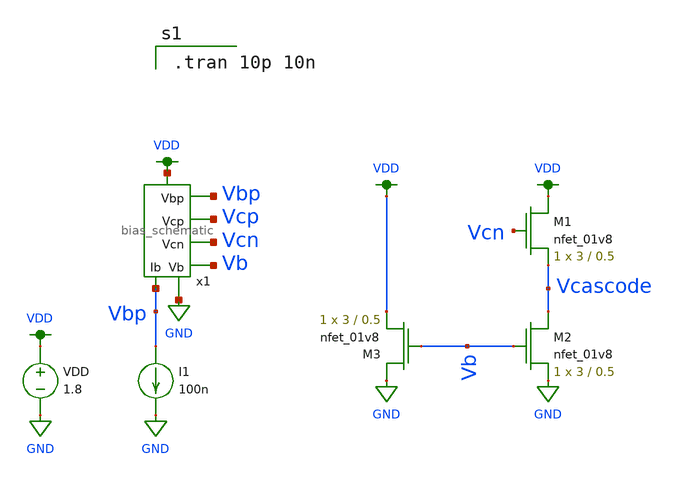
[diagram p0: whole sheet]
** sch_path: mp3/xschem/test_bias.sch
**.subckt test_bias
x1 VDD Vbp Vbp Vcp Vcn GND Vb bias_schematic
I1 Vbp GND 100n
VDD VDD GND 1.8
XM1 VDD Vcn Vcascode GND sky130_fd_pr__nfet_01v8 L=0.5 W=3 nf=1 ad='int((nf+1)/2) * W/nf * 0.29' as='int((nf+2)/2) * W/nf * 0.29'
+ pd='2*int((nf+1)/2) * (W/nf + 0.29)' ps='2*int((nf+2)/2) * (W/nf + 0.29)' nrd='0.29 / W' nrs='0.29 / W'
+ sa=0 sb=0 sd=0 mult=1 m=1
XM2 Vcascode Vb GND GND sky130_fd_pr__nfet_01v8 L=0.5 W=3 nf=1 ad='int((nf+1)/2) * W/nf * 0.29' as='int((nf+2)/2) * W/nf * 0.29'
+ pd='2*int((nf+1)/2) * (W/nf + 0.29)' ps='2*int((nf+2)/2) * (W/nf + 0.29)' nrd='0.29 / W' nrs='0.29 / W'
+ sa=0 sb=0 sd=0 mult=1 m=1
XM3 GND Vb VDD GND sky130_fd_pr__nfet_01v8 L=0.5 W=3 nf=1 ad='int((nf+1)/2) * W/nf * 0.29' as='int((nf+2)/2) * W/nf * 0.29'
+ pd='2*int((nf+1)/2) * (W/nf + 0.29)' ps='2*int((nf+2)/2) * (W/nf + 0.29)' nrd='0.29 / W' nrs='0.29 / W'
+ sa=0 sb=0 sd=0 mult=1 m=1
**** begin user architecture code

.option wnflag=1
.lib ~/skywater/skywater-pdk/libraries/sky130_fd_pr_ngspice/latest/models/sky130.lib.spice tt


.tran 10p 10n

**** end user architecture code
**.ends

* expanding   symbol:  /home/madvlsi/dev/git/vlsi/mp3/xschem/bias_schematic.sym # of pins=7
** sym_path: mp3/debug_files/bias_schematic.sym
** sch_path: mp3/debug_files/bias_schematic.sch
.subckt bias_schematic VP Vbp Ib Vcp Vcn VN Vb
*.iopin VP
*.iopin VN
*.iopin Ib
*.opin Vcp
*.opin Vbp
*.opin Vcn
*.opin Vb
XM1a net2 net2 net1 GND sky130_fd_pr__nfet_01v8 L=0.5 W=30 nf=1 ad='int((nf+1)/2) * W/nf * 0.29' as='int((nf+2)/2) * W/nf * 0.29'
+ pd='2*int((nf+1)/2) * (W/nf + 0.29)' ps='2*int((nf+2)/2) * (W/nf + 0.29)' nrd='0.29 / W' nrs='0.29 / W'
+ sa=0 sb=0 sd=0 mult=1 m=1
XM1b net2 net2 net1 GND sky130_fd_pr__nfet_01v8 L=0.5 W=30 nf=1 ad='int((nf+1)/2) * W/nf * 0.29' as='int((nf+2)/2) * W/nf * 0.29'
+ pd='2*int((nf+1)/2) * (W/nf + 0.29)' ps='2*int((nf+2)/2) * (W/nf + 0.29)' nrd='0.29 / W' nrs='0.29 / W'
+ sa=0 sb=0 sd=0 mult=1 m=1
XM1c net2 net2 net1 GND sky130_fd_pr__nfet_01v8 L=0.5 W=30 nf=1 ad='int((nf+1)/2) * W/nf * 0.29' as='int((nf+2)/2) * W/nf * 0.29'
+ pd='2*int((nf+1)/2) * (W/nf + 0.29)' ps='2*int((nf+2)/2) * (W/nf + 0.29)' nrd='0.29 / W' nrs='0.29 / W'
+ sa=0 sb=0 sd=0 mult=1 m=1
XM1d net2 net2 net1 GND sky130_fd_pr__nfet_01v8 L=0.5 W=30 nf=1 ad='int((nf+1)/2) * W/nf * 0.29' as='int((nf+2)/2) * W/nf * 0.29'
+ pd='2*int((nf+1)/2) * (W/nf + 0.29)' ps='2*int((nf+2)/2) * (W/nf + 0.29)' nrd='0.29 / W' nrs='0.29 / W'
+ sa=0 sb=0 sd=0 mult=1 m=1
XM2a VN net2 net1 GND sky130_fd_pr__nfet_01v8 L=0.5 W=3 nf=1 ad='int((nf+1)/2) * W/nf * 0.29' as='int((nf+2)/2) * W/nf * 0.29'
+ pd='2*int((nf+1)/2) * (W/nf + 0.29)' ps='2*int((nf+2)/2) * (W/nf + 0.29)' nrd='0.29 / W' nrs='0.29 / W'
+ sa=0 sb=0 sd=0 mult=1 m=1
XM2b VN net2 net1 GND sky130_fd_pr__nfet_01v8 L=0.5 W=3 nf=1 ad='int((nf+1)/2) * W/nf * 0.29' as='int((nf+2)/2) * W/nf * 0.29'
+ pd='2*int((nf+1)/2) * (W/nf + 0.29)' ps='2*int((nf+2)/2) * (W/nf + 0.29)' nrd='0.29 / W' nrs='0.29 / W'
+ sa=0 sb=0 sd=0 mult=1 m=1
XM2c VN net2 net1 GND sky130_fd_pr__nfet_01v8 L=0.5 W=3 nf=1 ad='int((nf+1)/2) * W/nf * 0.29' as='int((nf+2)/2) * W/nf * 0.29'
+ pd='2*int((nf+1)/2) * (W/nf + 0.29)' ps='2*int((nf+2)/2) * (W/nf + 0.29)' nrd='0.29 / W' nrs='0.29 / W'
+ sa=0 sb=0 sd=0 mult=1 m=1
XM2d VN net2 net1 GND sky130_fd_pr__nfet_01v8 L=0.5 W=3 nf=1 ad='int((nf+1)/2) * W/nf * 0.29' as='int((nf+2)/2) * W/nf * 0.29'
+ pd='2*int((nf+1)/2) * (W/nf + 0.29)' ps='2*int((nf+2)/2) * (W/nf + 0.29)' nrd='0.29 / W' nrs='0.29 / W'
+ sa=0 sb=0 sd=0 mult=1 m=1
XM3a net2 Ib VP VDD sky130_fd_pr__pfet_01v8 L=0.5 W=3 nf=1 ad='int((nf+1)/2) * W/nf * 0.29' as='int((nf+2)/2) * W/nf * 0.29'
+ pd='2*int((nf+1)/2) * (W/nf + 0.29)' ps='2*int((nf+2)/2) * (W/nf + 0.29)' nrd='0.29 / W' nrs='0.29 / W'
+ sa=0 sb=0 sd=0 mult=1 m=1
XM3b net2 Ib VP VDD sky130_fd_pr__pfet_01v8 L=0.5 W=3 nf=1 ad='int((nf+1)/2) * W/nf * 0.29' as='int((nf+2)/2) * W/nf * 0.29'
+ pd='2*int((nf+1)/2) * (W/nf + 0.29)' ps='2*int((nf+2)/2) * (W/nf + 0.29)' nrd='0.29 / W' nrs='0.29 / W'
+ sa=0 sb=0 sd=0 mult=1 m=1
XM3c net2 Ib VP VDD sky130_fd_pr__pfet_01v8 L=0.5 W=3 nf=1 ad='int((nf+1)/2) * W/nf * 0.29' as='int((nf+2)/2) * W/nf * 0.29'
+ pd='2*int((nf+1)/2) * (W/nf + 0.29)' ps='2*int((nf+2)/2) * (W/nf + 0.29)' nrd='0.29 / W' nrs='0.29 / W'
+ sa=0 sb=0 sd=0 mult=1 m=1
XM3d net2 Ib VP VDD sky130_fd_pr__pfet_01v8 L=0.5 W=3 nf=1 ad='int((nf+1)/2) * W/nf * 0.29' as='int((nf+2)/2) * W/nf * 0.29'
+ pd='2*int((nf+1)/2) * (W/nf + 0.29)' ps='2*int((nf+2)/2) * (W/nf + 0.29)' nrd='0.29 / W' nrs='0.29 / W'
+ sa=0 sb=0 sd=0 mult=1 m=1
XM4a Vcn Ib VP VDD sky130_fd_pr__pfet_01v8 L=0.5 W=30 nf=1 ad='int((nf+1)/2) * W/nf * 0.29' as='int((nf+2)/2) * W/nf * 0.29'
+ pd='2*int((nf+1)/2) * (W/nf + 0.29)' ps='2*int((nf+2)/2) * (W/nf + 0.29)' nrd='0.29 / W' nrs='0.29 / W'
+ sa=0 sb=0 sd=0 mult=1 m=1
XM4b Vcn Ib VP VDD sky130_fd_pr__pfet_01v8 L=0.5 W=30 nf=1 ad='int((nf+1)/2) * W/nf * 0.29' as='int((nf+2)/2) * W/nf * 0.29'
+ pd='2*int((nf+1)/2) * (W/nf + 0.29)' ps='2*int((nf+2)/2) * (W/nf + 0.29)' nrd='0.29 / W' nrs='0.29 / W'
+ sa=0 sb=0 sd=0 mult=1 m=1
XM4c Vcn Ib VP VDD sky130_fd_pr__pfet_01v8 L=0.5 W=30 nf=1 ad='int((nf+1)/2) * W/nf * 0.29' as='int((nf+2)/2) * W/nf * 0.29'
+ pd='2*int((nf+1)/2) * (W/nf + 0.29)' ps='2*int((nf+2)/2) * (W/nf + 0.29)' nrd='0.29 / W' nrs='0.29 / W'
+ sa=0 sb=0 sd=0 mult=1 m=1
XM4d Vcn Ib VP VDD sky130_fd_pr__pfet_01v8 L=0.5 W=30 nf=1 ad='int((nf+1)/2) * W/nf * 0.29' as='int((nf+2)/2) * W/nf * 0.29'
+ pd='2*int((nf+1)/2) * (W/nf + 0.29)' ps='2*int((nf+2)/2) * (W/nf + 0.29)' nrd='0.29 / W' nrs='0.29 / W'
+ sa=0 sb=0 sd=0 mult=1 m=1
XM11a Ib Ib VP VDD sky130_fd_pr__pfet_01v8 L=0.5 W=3 nf=1 ad='int((nf+1)/2) * W/nf * 0.29' as='int((nf+2)/2) * W/nf * 0.29'
+ pd='2*int((nf+1)/2) * (W/nf + 0.29)' ps='2*int((nf+2)/2) * (W/nf + 0.29)' nrd='0.29 / W' nrs='0.29 / W'
+ sa=0 sb=0 sd=0 mult=1 m=1
XM11b Ib Ib VP VDD sky130_fd_pr__pfet_01v8 L=0.5 W=3 nf=1 ad='int((nf+1)/2) * W/nf * 0.29' as='int((nf+2)/2) * W/nf * 0.29'
+ pd='2*int((nf+1)/2) * (W/nf + 0.29)' ps='2*int((nf+2)/2) * (W/nf + 0.29)' nrd='0.29 / W' nrs='0.29 / W'
+ sa=0 sb=0 sd=0 mult=1 m=1
XM11c Ib Ib VP VDD sky130_fd_pr__pfet_01v8 L=0.5 W=3 nf=1 ad='int((nf+1)/2) * W/nf * 0.29' as='int((nf+2)/2) * W/nf * 0.29'
+ pd='2*int((nf+1)/2) * (W/nf + 0.29)' ps='2*int((nf+2)/2) * (W/nf + 0.29)' nrd='0.29 / W' nrs='0.29 / W'
+ sa=0 sb=0 sd=0 mult=1 m=1
XM11d Ib Ib VP VDD sky130_fd_pr__pfet_01v8 L=0.5 W=3 nf=1 ad='int((nf+1)/2) * W/nf * 0.29' as='int((nf+2)/2) * W/nf * 0.29'
+ pd='2*int((nf+1)/2) * (W/nf + 0.29)' ps='2*int((nf+2)/2) * (W/nf + 0.29)' nrd='0.29 / W' nrs='0.29 / W'
+ sa=0 sb=0 sd=0 mult=1 m=1
XM5a net1 Vcn Vcn GND sky130_fd_pr__nfet_01v8 L=0.5 W=30 nf=1 ad='int((nf+1)/2) * W/nf * 0.29' as='int((nf+2)/2) * W/nf * 0.29'
+ pd='2*int((nf+1)/2) * (W/nf + 0.29)' ps='2*int((nf+2)/2) * (W/nf + 0.29)' nrd='0.29 / W' nrs='0.29 / W'
+ sa=0 sb=0 sd=0 mult=1 m=1
XM5b net1 Vcn Vcn GND sky130_fd_pr__nfet_01v8 L=0.5 W=30 nf=1 ad='int((nf+1)/2) * W/nf * 0.29' as='int((nf+2)/2) * W/nf * 0.29'
+ pd='2*int((nf+1)/2) * (W/nf + 0.29)' ps='2*int((nf+2)/2) * (W/nf + 0.29)' nrd='0.29 / W' nrs='0.29 / W'
+ sa=0 sb=0 sd=0 mult=1 m=1
XM5c net1 Vcn Vcn GND sky130_fd_pr__nfet_01v8 L=0.5 W=30 nf=1 ad='int((nf+1)/2) * W/nf * 0.29' as='int((nf+2)/2) * W/nf * 0.29'
+ pd='2*int((nf+1)/2) * (W/nf + 0.29)' ps='2*int((nf+2)/2) * (W/nf + 0.29)' nrd='0.29 / W' nrs='0.29 / W'
+ sa=0 sb=0 sd=0 mult=1 m=1
XM5d net1 Vcn Vcn GND sky130_fd_pr__nfet_01v8 L=0.5 W=30 nf=1 ad='int((nf+1)/2) * W/nf * 0.29' as='int((nf+2)/2) * W/nf * 0.29'
+ pd='2*int((nf+1)/2) * (W/nf + 0.29)' ps='2*int((nf+2)/2) * (W/nf + 0.29)' nrd='0.29 / W' nrs='0.29 / W'
+ sa=0 sb=0 sd=0 mult=1 m=1
XM8a VN Vb net3 GND sky130_fd_pr__nfet_01v8 L=0.5 W=3 nf=1 ad='int((nf+1)/2) * W/nf * 0.29' as='int((nf+2)/2) * W/nf * 0.29'
+ pd='2*int((nf+1)/2) * (W/nf + 0.29)' ps='2*int((nf+2)/2) * (W/nf + 0.29)' nrd='0.29 / W' nrs='0.29 / W'
+ sa=0 sb=0 sd=0 mult=1 m=1
XM8b VN Vb net3 GND sky130_fd_pr__nfet_01v8 L=0.5 W=3 nf=1 ad='int((nf+1)/2) * W/nf * 0.29' as='int((nf+2)/2) * W/nf * 0.29'
+ pd='2*int((nf+1)/2) * (W/nf + 0.29)' ps='2*int((nf+2)/2) * (W/nf + 0.29)' nrd='0.29 / W' nrs='0.29 / W'
+ sa=0 sb=0 sd=0 mult=1 m=1
XM8c VN Vb net3 GND sky130_fd_pr__nfet_01v8 L=0.5 W=3 nf=1 ad='int((nf+1)/2) * W/nf * 0.29' as='int((nf+2)/2) * W/nf * 0.29'
+ pd='2*int((nf+1)/2) * (W/nf + 0.29)' ps='2*int((nf+2)/2) * (W/nf + 0.29)' nrd='0.29 / W' nrs='0.29 / W'
+ sa=0 sb=0 sd=0 mult=1 m=1
XM8d VN Vb net3 GND sky130_fd_pr__nfet_01v8 L=0.5 W=3 nf=1 ad='int((nf+1)/2) * W/nf * 0.29' as='int((nf+2)/2) * W/nf * 0.29'
+ pd='2*int((nf+1)/2) * (W/nf + 0.29)' ps='2*int((nf+2)/2) * (W/nf + 0.29)' nrd='0.29 / W' nrs='0.29 / W'
+ sa=0 sb=0 sd=0 mult=1 m=1
XM6a net3 net3 net4 VDD sky130_fd_pr__pfet_01v8 L=0.5 W=30 nf=1 ad='int((nf+1)/2) * W/nf * 0.29' as='int((nf+2)/2) * W/nf * 0.29'
+ pd='2*int((nf+1)/2) * (W/nf + 0.29)' ps='2*int((nf+2)/2) * (W/nf + 0.29)' nrd='0.29 / W' nrs='0.29 / W'
+ sa=0 sb=0 sd=0 mult=1 m=1
XM6b net3 net3 net4 VDD sky130_fd_pr__pfet_01v8 L=0.5 W=30 nf=1 ad='int((nf+1)/2) * W/nf * 0.29' as='int((nf+2)/2) * W/nf * 0.29'
+ pd='2*int((nf+1)/2) * (W/nf + 0.29)' ps='2*int((nf+2)/2) * (W/nf + 0.29)' nrd='0.29 / W' nrs='0.29 / W'
+ sa=0 sb=0 sd=0 mult=1 m=1
XM6c net3 net3 net4 VDD sky130_fd_pr__pfet_01v8 L=0.5 W=30 nf=1 ad='int((nf+1)/2) * W/nf * 0.29' as='int((nf+2)/2) * W/nf * 0.29'
+ pd='2*int((nf+1)/2) * (W/nf + 0.29)' ps='2*int((nf+2)/2) * (W/nf + 0.29)' nrd='0.29 / W' nrs='0.29 / W'
+ sa=0 sb=0 sd=0 mult=1 m=1
XM6d net3 net3 net4 VDD sky130_fd_pr__pfet_01v8 L=0.5 W=30 nf=1 ad='int((nf+1)/2) * W/nf * 0.29' as='int((nf+2)/2) * W/nf * 0.29'
+ pd='2*int((nf+1)/2) * (W/nf + 0.29)' ps='2*int((nf+2)/2) * (W/nf + 0.29)' nrd='0.29 / W' nrs='0.29 / W'
+ sa=0 sb=0 sd=0 mult=1 m=1
XM7a net4 net3 VP VDD sky130_fd_pr__pfet_01v8 L=0.5 W=3 nf=1 ad='int((nf+1)/2) * W/nf * 0.29' as='int((nf+2)/2) * W/nf * 0.29'
+ pd='2*int((nf+1)/2) * (W/nf + 0.29)' ps='2*int((nf+2)/2) * (W/nf + 0.29)' nrd='0.29 / W' nrs='0.29 / W'
+ sa=0 sb=0 sd=0 mult=1 m=1
XM7b net4 net3 VP VDD sky130_fd_pr__pfet_01v8 L=0.5 W=3 nf=1 ad='int((nf+1)/2) * W/nf * 0.29' as='int((nf+2)/2) * W/nf * 0.29'
+ pd='2*int((nf+1)/2) * (W/nf + 0.29)' ps='2*int((nf+2)/2) * (W/nf + 0.29)' nrd='0.29 / W' nrs='0.29 / W'
+ sa=0 sb=0 sd=0 mult=1 m=1
XM7c net4 net3 VP VDD sky130_fd_pr__pfet_01v8 L=0.5 W=3 nf=1 ad='int((nf+1)/2) * W/nf * 0.29' as='int((nf+2)/2) * W/nf * 0.29'
+ pd='2*int((nf+1)/2) * (W/nf + 0.29)' ps='2*int((nf+2)/2) * (W/nf + 0.29)' nrd='0.29 / W' nrs='0.29 / W'
+ sa=0 sb=0 sd=0 mult=1 m=1
XM7d net4 net3 VP VDD sky130_fd_pr__pfet_01v8 L=0.5 W=3 nf=1 ad='int((nf+1)/2) * W/nf * 0.29' as='int((nf+2)/2) * W/nf * 0.29'
+ pd='2*int((nf+1)/2) * (W/nf + 0.29)' ps='2*int((nf+2)/2) * (W/nf + 0.29)' nrd='0.29 / W' nrs='0.29 / W'
+ sa=0 sb=0 sd=0 mult=1 m=1
XM10d net4 Vcp Vcp VDD sky130_fd_pr__pfet_01v8 L=0.5 W=30 nf=1 ad='int((nf+1)/2) * W/nf * 0.29' as='int((nf+2)/2) * W/nf * 0.29'
+ pd='2*int((nf+1)/2) * (W/nf + 0.29)' ps='2*int((nf+2)/2) * (W/nf + 0.29)' nrd='0.29 / W' nrs='0.29 / W'
+ sa=0 sb=0 sd=0 mult=1 m=1
XM10c net4 Vcp Vcp VDD sky130_fd_pr__pfet_01v8 L=0.5 W=30 nf=1 ad='int((nf+1)/2) * W/nf * 0.29' as='int((nf+2)/2) * W/nf * 0.29'
+ pd='2*int((nf+1)/2) * (W/nf + 0.29)' ps='2*int((nf+2)/2) * (W/nf + 0.29)' nrd='0.29 / W' nrs='0.29 / W'
+ sa=0 sb=0 sd=0 mult=1 m=1
XM10b net4 Vcp Vcp VDD sky130_fd_pr__pfet_01v8 L=0.5 W=30 nf=1 ad='int((nf+1)/2) * W/nf * 0.29' as='int((nf+2)/2) * W/nf * 0.29'
+ pd='2*int((nf+1)/2) * (W/nf + 0.29)' ps='2*int((nf+2)/2) * (W/nf + 0.29)' nrd='0.29 / W' nrs='0.29 / W'
+ sa=0 sb=0 sd=0 mult=1 m=1
XM10a net4 Vcp Vcp VDD sky130_fd_pr__pfet_01v8 L=0.5 W=30 nf=1 ad='int((nf+1)/2) * W/nf * 0.29' as='int((nf+2)/2) * W/nf * 0.29'
+ pd='2*int((nf+1)/2) * (W/nf + 0.29)' ps='2*int((nf+2)/2) * (W/nf + 0.29)' nrd='0.29 / W' nrs='0.29 / W'
+ sa=0 sb=0 sd=0 mult=1 m=1
XM9a VN Vb Vcp GND sky130_fd_pr__nfet_01v8 L=0.5 W=30 nf=1 ad='int((nf+1)/2) * W/nf * 0.29' as='int((nf+2)/2) * W/nf * 0.29'
+ pd='2*int((nf+1)/2) * (W/nf + 0.29)' ps='2*int((nf+2)/2) * (W/nf + 0.29)' nrd='0.29 / W' nrs='0.29 / W'
+ sa=0 sb=0 sd=0 mult=1 m=1
XM9b VN Vb Vcp GND sky130_fd_pr__nfet_01v8 L=0.5 W=30 nf=1 ad='int((nf+1)/2) * W/nf * 0.29' as='int((nf+2)/2) * W/nf * 0.29'
+ pd='2*int((nf+1)/2) * (W/nf + 0.29)' ps='2*int((nf+2)/2) * (W/nf + 0.29)' nrd='0.29 / W' nrs='0.29 / W'
+ sa=0 sb=0 sd=0 mult=1 m=1
XM9c VN Vb Vcp GND sky130_fd_pr__nfet_01v8 L=0.5 W=30 nf=1 ad='int((nf+1)/2) * W/nf * 0.29' as='int((nf+2)/2) * W/nf * 0.29'
+ pd='2*int((nf+1)/2) * (W/nf + 0.29)' ps='2*int((nf+2)/2) * (W/nf + 0.29)' nrd='0.29 / W' nrs='0.29 / W'
+ sa=0 sb=0 sd=0 mult=1 m=1
XM9d VN Vb Vcp GND sky130_fd_pr__nfet_01v8 L=0.5 W=30 nf=1 ad='int((nf+1)/2) * W/nf * 0.29' as='int((nf+2)/2) * W/nf * 0.29'
+ pd='2*int((nf+1)/2) * (W/nf + 0.29)' ps='2*int((nf+2)/2) * (W/nf + 0.29)' nrd='0.29 / W' nrs='0.29 / W'
+ sa=0 sb=0 sd=0 mult=1 m=1
XM12a VN Vb Vb GND sky130_fd_pr__nfet_01v8 L=0.5 W=3 nf=1 ad='int((nf+1)/2) * W/nf * 0.29' as='int((nf+2)/2) * W/nf * 0.29'
+ pd='2*int((nf+1)/2) * (W/nf + 0.29)' ps='2*int((nf+2)/2) * (W/nf + 0.29)' nrd='0.29 / W' nrs='0.29 / W'
+ sa=0 sb=0 sd=0 mult=1 m=1
XM12b VN Vb Vb GND sky130_fd_pr__nfet_01v8 L=0.5 W=3 nf=1 ad='int((nf+1)/2) * W/nf * 0.29' as='int((nf+2)/2) * W/nf * 0.29'
+ pd='2*int((nf+1)/2) * (W/nf + 0.29)' ps='2*int((nf+2)/2) * (W/nf + 0.29)' nrd='0.29 / W' nrs='0.29 / W'
+ sa=0 sb=0 sd=0 mult=1 m=1
XM12c VN Vb Vb GND sky130_fd_pr__nfet_01v8 L=0.5 W=3 nf=1 ad='int((nf+1)/2) * W/nf * 0.29' as='int((nf+2)/2) * W/nf * 0.29'
+ pd='2*int((nf+1)/2) * (W/nf + 0.29)' ps='2*int((nf+2)/2) * (W/nf + 0.29)' nrd='0.29 / W' nrs='0.29 / W'
+ sa=0 sb=0 sd=0 mult=1 m=1
XM12d VN Vb Vb GND sky130_fd_pr__nfet_01v8 L=0.5 W=3 nf=1 ad='int((nf+1)/2) * W/nf * 0.29' as='int((nf+2)/2) * W/nf * 0.29'
+ pd='2*int((nf+1)/2) * (W/nf + 0.29)' ps='2*int((nf+2)/2) * (W/nf + 0.29)' nrd='0.29 / W' nrs='0.29 / W'
+ sa=0 sb=0 sd=0 mult=1 m=1
XM1 Vb Ib VP VDD sky130_fd_pr__pfet_01v8 L=0.5 W=3 nf=1 ad='int((nf+1)/2) * W/nf * 0.29' as='int((nf+2)/2) * W/nf * 0.29'
+ pd='2*int((nf+1)/2) * (W/nf + 0.29)' ps='2*int((nf+2)/2) * (W/nf + 0.29)' nrd='0.29 / W' nrs='0.29 / W'
+ sa=0 sb=0 sd=0 mult=1 m=1
XM2 Vb Ib VP VDD sky130_fd_pr__pfet_01v8 L=0.5 W=3 nf=1 ad='int((nf+1)/2) * W/nf * 0.29' as='int((nf+2)/2) * W/nf * 0.29'
+ pd='2*int((nf+1)/2) * (W/nf + 0.29)' ps='2*int((nf+2)/2) * (W/nf + 0.29)' nrd='0.29 / W' nrs='0.29 / W'
+ sa=0 sb=0 sd=0 mult=1 m=1
XM3 Vb Ib VP VDD sky130_fd_pr__pfet_01v8 L=0.5 W=3 nf=1 ad='int((nf+1)/2) * W/nf * 0.29' as='int((nf+2)/2) * W/nf * 0.29'
+ pd='2*int((nf+1)/2) * (W/nf + 0.29)' ps='2*int((nf+2)/2) * (W/nf + 0.29)' nrd='0.29 / W' nrs='0.29 / W'
+ sa=0 sb=0 sd=0 mult=1 m=1
XM4 Vb Ib VP VDD sky130_fd_pr__pfet_01v8 L=0.5 W=3 nf=1 ad='int((nf+1)/2) * W/nf * 0.29' as='int((nf+2)/2) * W/nf * 0.29'
+ pd='2*int((nf+1)/2) * (W/nf + 0.29)' ps='2*int((nf+2)/2) * (W/nf + 0.29)' nrd='0.29 / W' nrs='0.29 / W'
+ sa=0 sb=0 sd=0 mult=1 m=1
.ends

.GLOBAL VDD
.GLOBAL GND
.end
